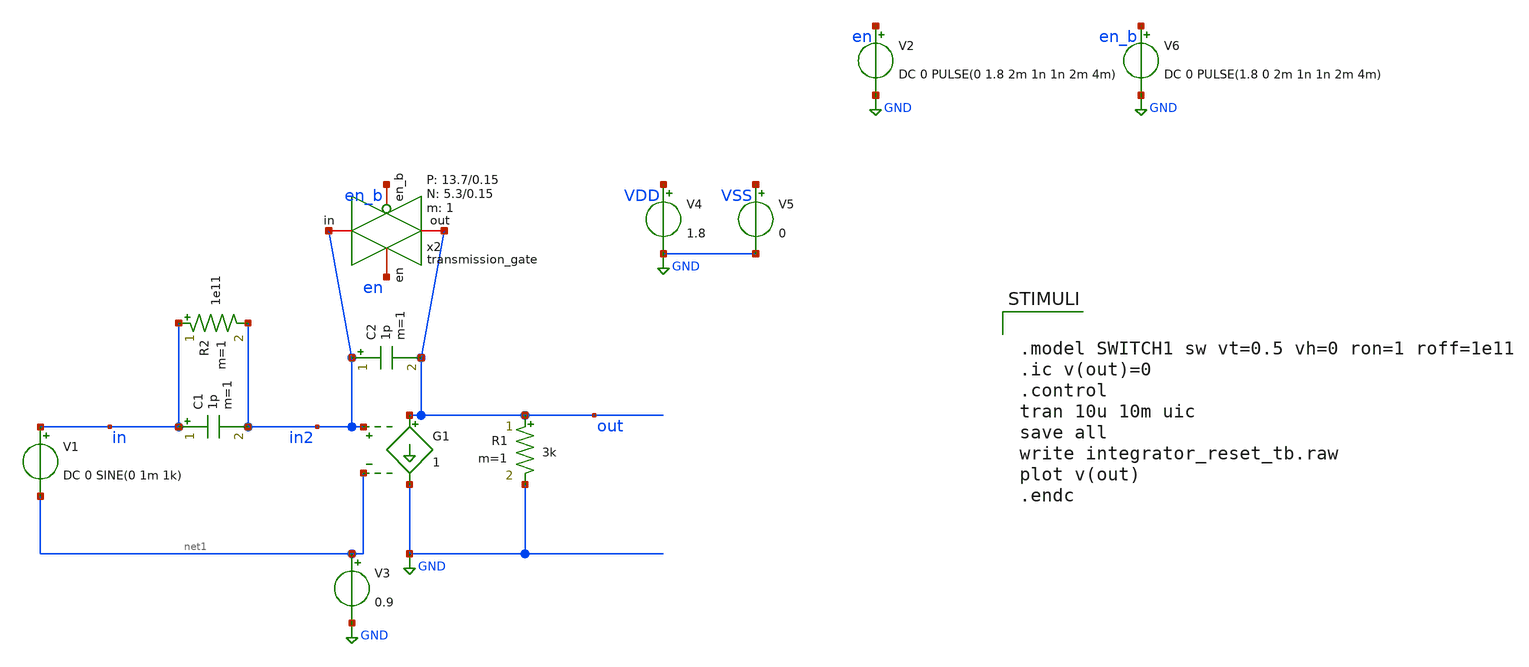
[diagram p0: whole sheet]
** sch_path: verification/analog_modulator/integrator_reset_tb.sch
**.subckt integrator_reset_tb
G1 out GND in2 net1 1
R1 out GND 3k m=1
V1 in net1 DC 0 SINE(0 1m 1k)
C1 in in2 1p m=1
C2 in2 out 1p m=1
V2 en GND DC 0 PULSE(0 1.8 2m 1n 1n 2m 4m)
V3 net1 GND 0.9
x2 in2 out en en_b VDD VSS 1 5.3 0.15 13.7 0.15 transmission_gate
V4 VDD GND 1.8
V5 VSS GND 0
V6 en_b GND DC 0 PULSE(1.8 0 2m 1n 1n 2m 4m)
R2 in in2 1e11 m=1
**** begin user architecture code

** opencircuitdesign pdks install
.lib /farmshare/home/classes/ee/372/PDKs/open_pdks_1.0.310/sky130/sky130A/libs.tech/ngspice/sky130.lib.spice tt
*.inc /farmshare/home/classes/ee/372/PDKs/open_pdks_1.0.310/sky130/sky130A/libs.ref/sky130_fd_sc_hd/spice/sky130_fd_sc_hd.spice



.model SWITCH1 sw vt=0.5 vh=0 ron=1 roff=1e11
.ic v(out)=0
.control
tran 10u 10m uic
save all
write integrator_reset_tb.raw
plot v(out)
.endc


**** end user architecture code
**.ends

* expanding   symbol:  transmission_gate.sym # of pins=4
** sym_path: design/schematic/transmission_gate.sym
** sch_path: design/schematic/transmission_gate.sch
.subckt transmission_gate in out en en_b VDD VSS N W_N L_N W_P L_P    N=1 W_N=5.3 L_N=0.15 W_P=13.7
+ L_P=0.15
*.iopin in
*.iopin out
*.ipin en
*.ipin en_b
XM1 out en in VSS sky130_fd_pr__nfet_01v8 L=L_N W=W_N nf=1 ad='int((nf+1)/2) * W/nf * 0.29' as='int((nf+2)/2) * W/nf * 0.29'
+ pd='2*int((nf+1)/2) * (W/nf + 0.29)' ps='2*int((nf+2)/2) * (W/nf + 0.29)' nrd='0.29 / W' nrs='0.29 / W'
+ sa=0 sb=0 sd=0 mult=N m=N
XM2 out en_b in VDD sky130_fd_pr__pfet_01v8 L=L_P W=W_P nf=1 ad='int((nf+1)/2) * W/nf * 0.29' as='int((nf+2)/2) * W/nf * 0.29'
+ pd='2*int((nf+1)/2) * (W/nf + 0.29)' ps='2*int((nf+2)/2) * (W/nf + 0.29)' nrd='0.29 / W' nrs='0.29 / W'
+ sa=0 sb=0 sd=0 mult=N m=N
.ends

.GLOBAL GND
.end
